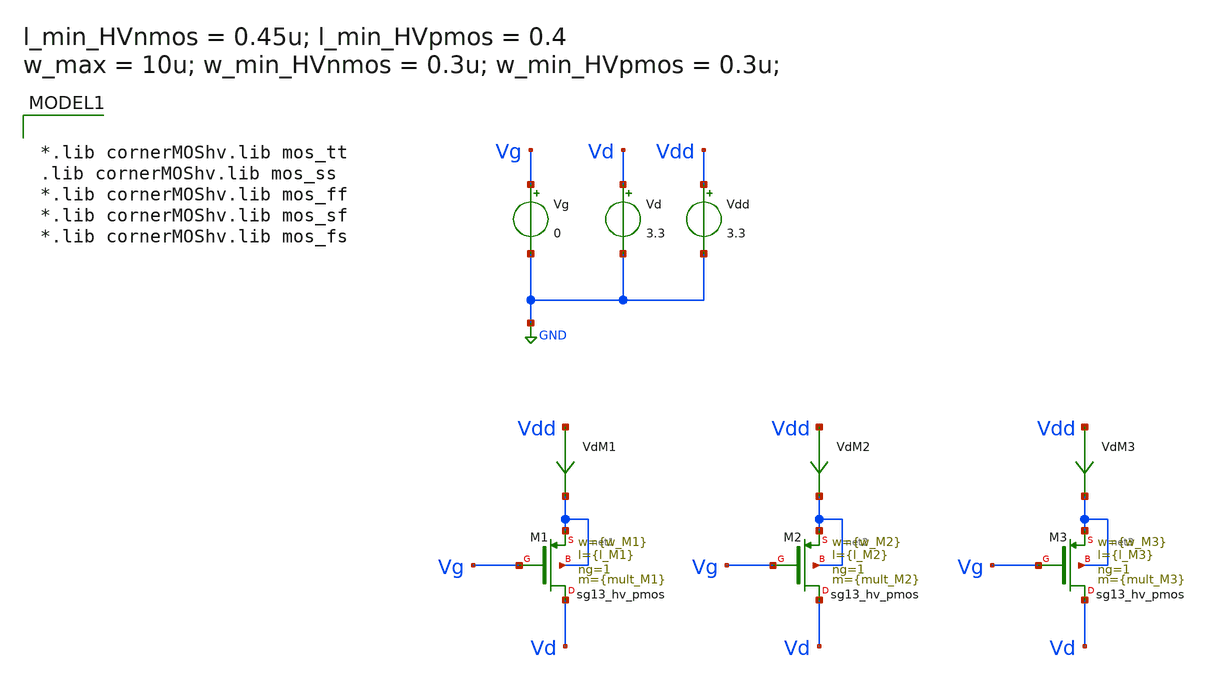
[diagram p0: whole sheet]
** sch_path: xschem/DCDCBuck/TB_hvPMOS_charact.sch
**.subckt TB_hvPMOS_charact
XM1 Vd Vg net1 net1 sg13_hv_pmos w={w_M1} l={l_M1} ng=1 m={mult_M1} mm_ok=1
Vg Vg GND 0
Vd Vd GND 3.3
Vdd Vdd GND 3.3
VdM1 Vdd net1 0
.save i(vdm1)
XM2 Vd Vg net2 net2 sg13_hv_pmos w={w_M2} l={l_M2} ng=1 m={mult_M2} mm_ok=1
VdM2 Vdd net2 0
.save i(vdm2)
XM3 Vd Vg net3 net3 sg13_hv_pmos w={w_M3} l={l_M3} ng=1 m={mult_M3} mm_ok=1
VdM3 Vdd net3 0
.save i(vdm3)
**** begin user architecture code


*.param temp=27
*.param temp=125
.option temp= 125

.param mult_M1 = 1200
.param w_M1 =10u
.param l_M1 =0.4u

.param mult_M2 = 1200
.param w_M2 =10u
.param l_M2 =0.45u

.param mult_M3 = 1200
.param w_M3 =10u
.param l_M3 =0.5u

.save all
* + @M.XM1.m1[id]  @n.xm1.nsg13_hv_pmos[vth]  @n.xm1.nsg13_hv_pmos[gds]  @n.xm2.nsg13_hv_pmos[vth]
*+  @n.xm2.nsg13_hv_pmos[gds]  @n.xm3.nsg13_hv_pmos[vth]  @n.xm3.nsg13_hv_pmos[gds]

.control
*dc Vd 0 3.3 0.01 Vg 0.5 3.3 0.5
*dc Vd 0 0.5 0.01 temp 0 27 1
dc Vd 0 3.3 0.01

let Vsd = v(Vdd) - v(Vd)
let G_M1 = @n.xm1.nsg13_hv_pmos[gds]
let G_M2 = @n.xm2.nsg13_hv_pmos[gds]
let G_M3 = @n.xm3.nsg13_hv_pmos[gds]
let Ron_M1 = 1/G_M1
let Ron_M2 = 1/G_M2
let Ron_M3 = 1/G_M3

plot i(VdM1) i(VdM2) i(VdM3) vs Vsd
plot Ron_M1 Ron_M2 Ron_M3 vs Vsd
*plot i(VdM1) i(VdM2) vs Vsd

*plot @n.xm1.nsg13_hv_pmos[vth] @n.xm2.nsg13_hv_pmos[vth] @n.xm3.nsg13_hv_pmos[vth]
*print @n.xm2.nsg13_hv_nmos[vth]
write test_pmos.raw
.endc


.control
reset
alter Vd 0
dc Vg 2 3.3 0.01
let Vsg = v(Vdd) - v(Vg)
plot i(VdM1) i(VdM2) i(VdM3) vs Vsg
.endc




*.lib cornerMOShv.lib mos_tt
.lib cornerMOShv.lib mos_ss
*.lib cornerMOShv.lib mos_ff
*.lib cornerMOShv.lib mos_sf
*.lib cornerMOShv.lib mos_fs

**** end user architecture code
**.ends
.GLOBAL GND
.end
